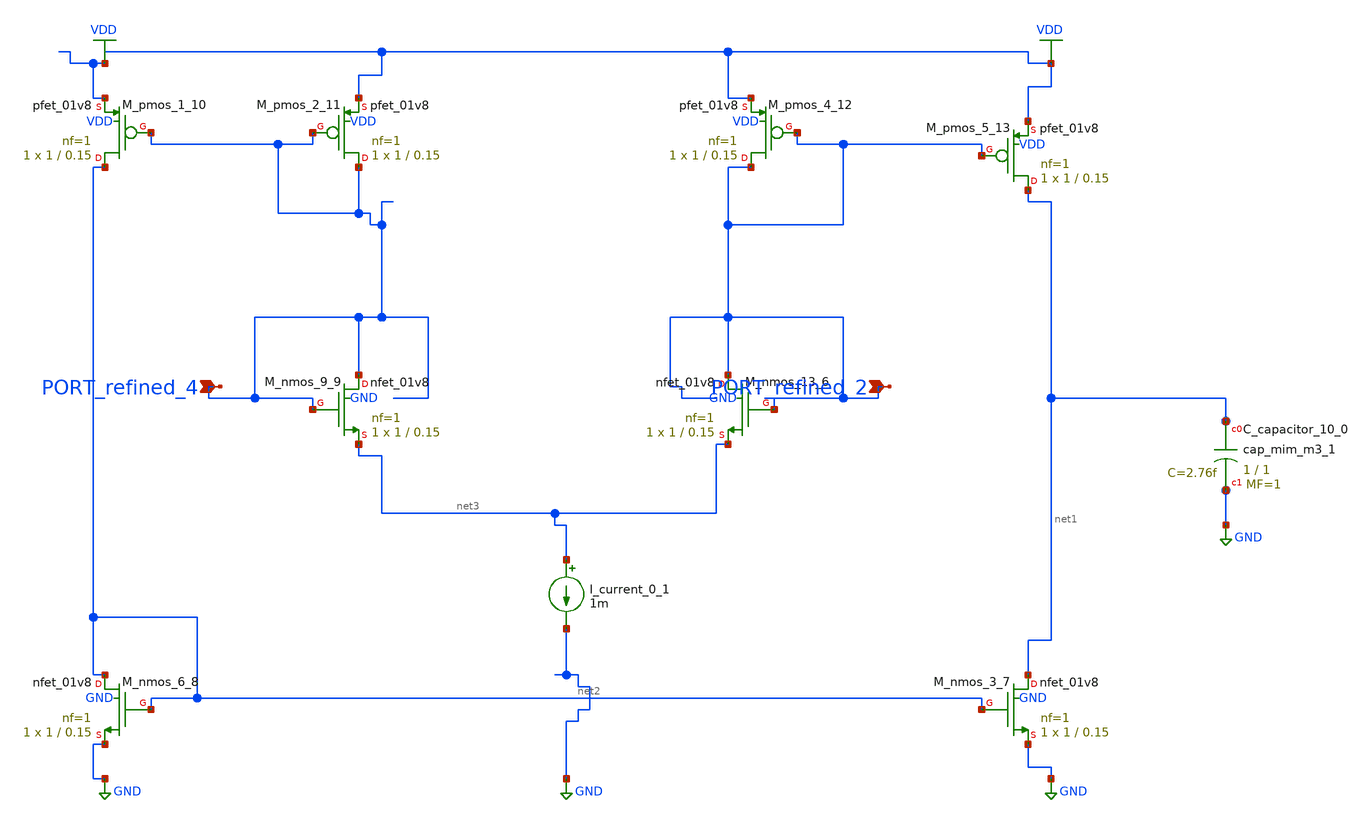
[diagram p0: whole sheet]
** sch_path: schematics/SchemGen/no_doi_01_002.sch
**.subckt no_doi_01_002 PORT_refined_2 PORT_refined_4
*.ipin PORT_refined_2
*.ipin PORT_refined_4
XC_capacitor_10_0 net1 GND sky130_fd_pr__cap_mim_m3_1 W=1 L=1 MF=1 m=1
I_current_0_1 net3 GND 1m
XM_nmos_13_6 PORT_refined_2 PORT_refined_2 net3 GND sky130_fd_pr__nfet_01v8 L=0.15 W=1 nf=1 ad='int((1 + 1)/2) * 1 / 1 * 0.29'
+ as='int((1 + 2)/2) * 1 / 1 * 0.29' pd='2*int((1 + 1)/2) * (1 / 1 + 0.29)' ps='2*int((1 + 2)/2) * (1 / 1 + 0.29)'
+ nrd='0.29 / 1 ' nrs='0.29 / 1 ' sa=0 sb=0 sd=0 mult=1 m=1
XM_nmos_3_7 net1 net2 GND GND sky130_fd_pr__nfet_01v8 L=0.15 W=1 nf=1 ad='int((1 + 1)/2) * 1 / 1 * 0.29'
+ as='int((1 + 2)/2) * 1 / 1 * 0.29' pd='2*int((1 + 1)/2) * (1 / 1 + 0.29)' ps='2*int((1 + 2)/2) * (1 / 1 + 0.29)'
+ nrd='0.29 / 1 ' nrs='0.29 / 1 ' sa=0 sb=0 sd=0 mult=1 m=1
XM_nmos_6_8 net2 net2 GND GND sky130_fd_pr__nfet_01v8 L=0.15 W=1 nf=1 ad='int((1 + 1)/2) * 1 / 1 * 0.29'
+ as='int((1 + 2)/2) * 1 / 1 * 0.29' pd='2*int((1 + 1)/2) * (1 / 1 + 0.29)' ps='2*int((1 + 2)/2) * (1 / 1 + 0.29)'
+ nrd='0.29 / 1 ' nrs='0.29 / 1 ' sa=0 sb=0 sd=0 mult=1 m=1
XM_nmos_9_9 PORT_refined_4 PORT_refined_4 net3 GND sky130_fd_pr__nfet_01v8 L=0.15 W=1 nf=1 ad='int((1 + 1)/2) * 1 / 1 * 0.29'
+ as='int((1 + 2)/2) * 1 / 1 * 0.29' pd='2*int((1 + 1)/2) * (1 / 1 + 0.29)' ps='2*int((1 + 2)/2) * (1 / 1 + 0.29)'
+ nrd='0.29 / 1 ' nrs='0.29 / 1 ' sa=0 sb=0 sd=0 mult=1 m=1
XM_pmos_1_10 net2 PORT_refined_4 VDD VDD sky130_fd_pr__pfet_01v8 L=0.15 W=1 nf=1 ad='int((1 + 1)/2) * 1 / 1 * 0.29'
+ as='int((1 + 2)/2) * 1 / 1 * 0.29' pd='2*int((1 + 1)/2) * (1 / 1 + 0.29)' ps='2*int((1 + 2)/2) * (1 / 1 + 0.29)'
+ nrd='0.29 / 1 ' nrs='0.29 / 1 ' sa=0 sb=0 sd=0 mult=1 m=1
XM_pmos_2_11 PORT_refined_4 PORT_refined_4 VDD VDD sky130_fd_pr__pfet_01v8 L=0.15 W=1 nf=1 ad='int((1 + 1)/2) * 1 / 1 * 0.29'
+ as='int((1 + 2)/2) * 1 / 1 * 0.29' pd='2*int((1 + 1)/2) * (1 / 1 + 0.29)' ps='2*int((1 + 2)/2) * (1 / 1 + 0.29)'
+ nrd='0.29 / 1 ' nrs='0.29 / 1 ' sa=0 sb=0 sd=0 mult=1 m=1
XM_pmos_4_12 PORT_refined_2 PORT_refined_2 VDD VDD sky130_fd_pr__pfet_01v8 L=0.15 W=1 nf=1 ad='int((1 + 1)/2) * 1 / 1 * 0.29'
+ as='int((1 + 2)/2) * 1 / 1 * 0.29' pd='2*int((1 + 1)/2) * (1 / 1 + 0.29)' ps='2*int((1 + 2)/2) * (1 / 1 + 0.29)'
+ nrd='0.29 / 1 ' nrs='0.29 / 1 ' sa=0 sb=0 sd=0 mult=1 m=1
XM_pmos_5_13 net1 PORT_refined_2 VDD VDD sky130_fd_pr__pfet_01v8 L=0.15 W=1 nf=1 ad='int((1 + 1)/2) * 1 / 1 * 0.29'
+ as='int((1 + 2)/2) * 1 / 1 * 0.29' pd='2*int((1 + 1)/2) * (1 / 1 + 0.29)' ps='2*int((1 + 2)/2) * (1 / 1 + 0.29)'
+ nrd='0.29 / 1 ' nrs='0.29 / 1 ' sa=0 sb=0 sd=0 mult=1 m=1
**.ends
.GLOBAL GND
.GLOBAL VDD
.end
